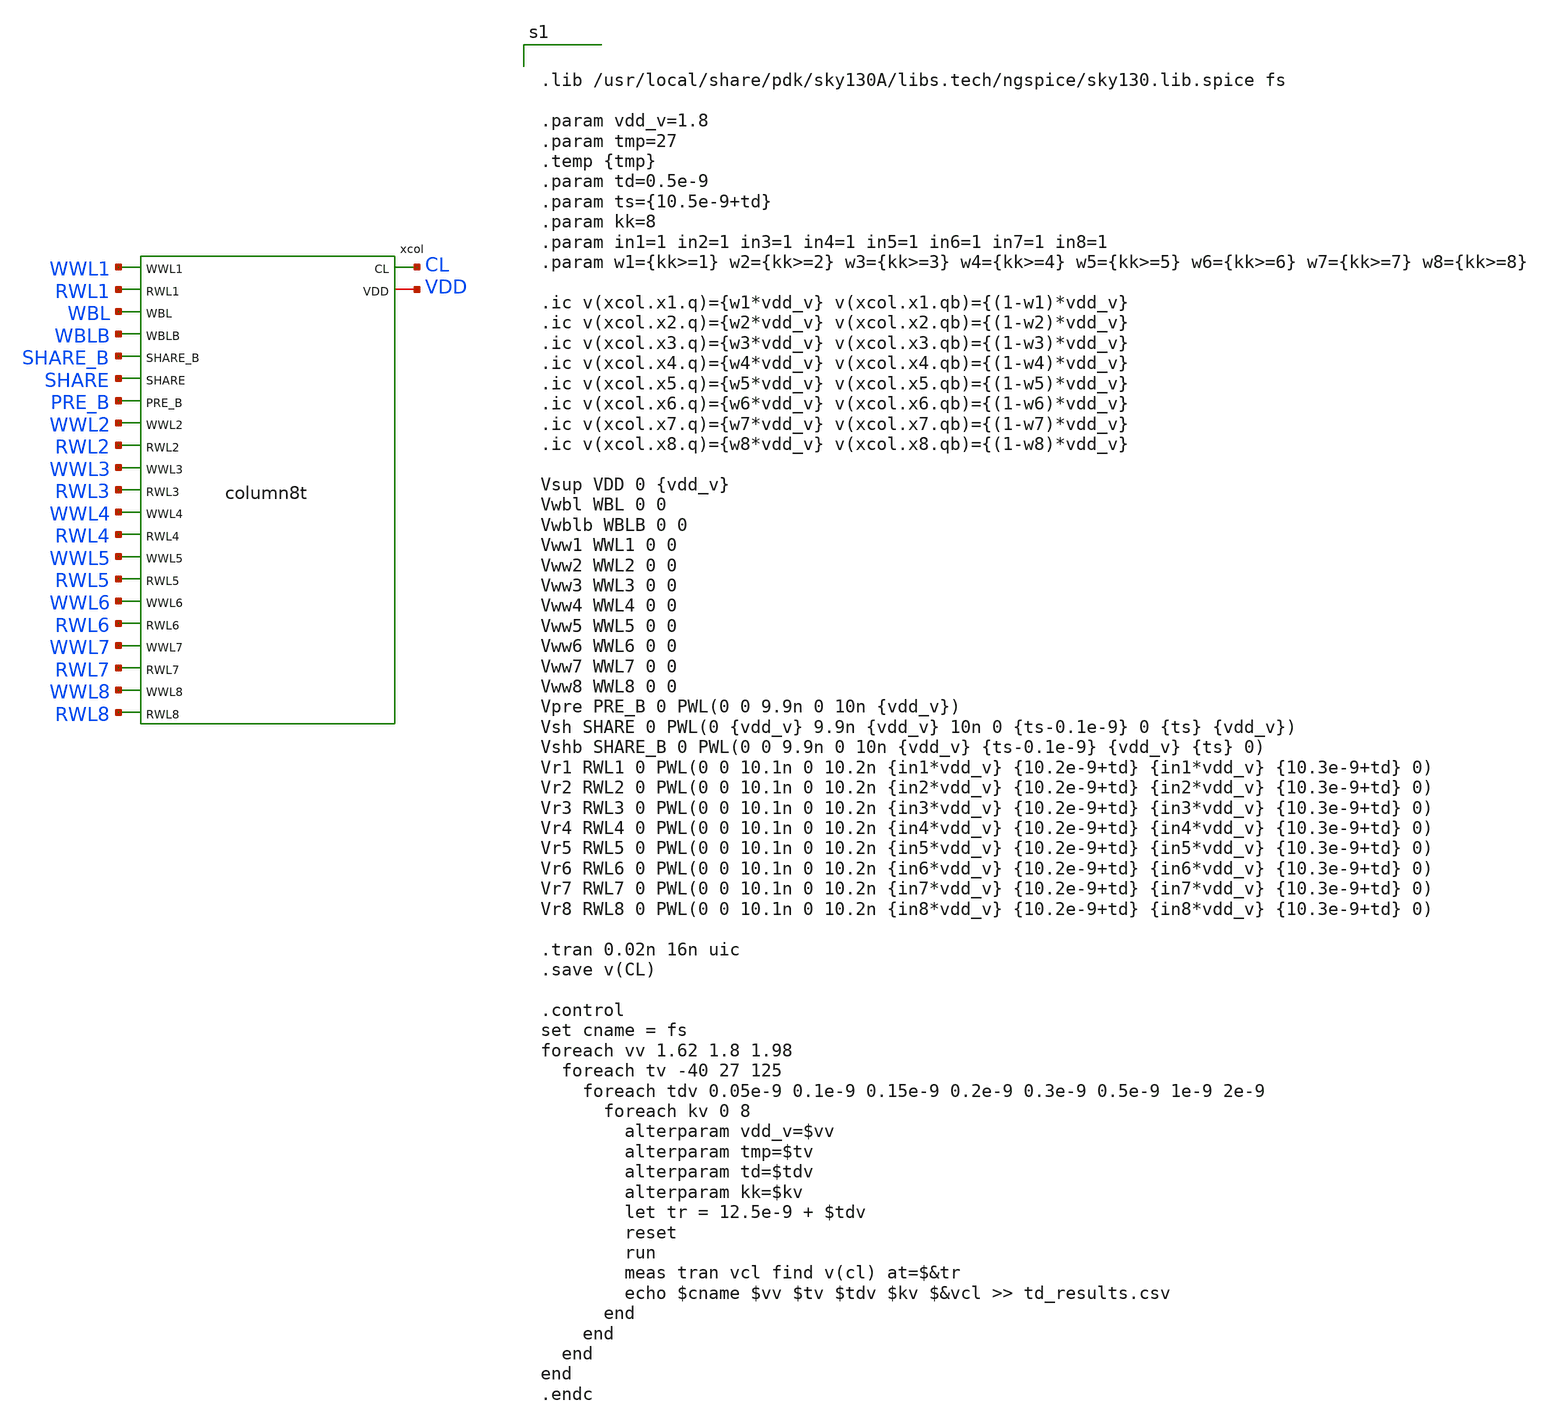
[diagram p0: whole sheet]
** sch_path: schematics/untitled-1.sch
**.subckt untitled-1
xcol CL VDD WWL1 RWL1 WBL WBLB SHARE_B SHARE PRE_B WWL2 RWL2 WWL3 RWL3 WWL4 RWL4 WWL5 RWL5 WWL6 RWL6
+ WWL7 RWL7 WWL8 RWL8 column8t
**** begin user architecture code


.lib /usr/local/share/pdk/sky130A/libs.tech/ngspice/sky130.lib.spice fs

.param vdd_v=1.8
.param tmp=27
.temp {tmp}
.param td=0.5e-9
.param ts={10.5e-9+td}
.param kk=8
.param in1=1 in2=1 in3=1 in4=1 in5=1 in6=1 in7=1 in8=1
.param w1={kk>=1} w2={kk>=2} w3={kk>=3} w4={kk>=4} w5={kk>=5} w6={kk>=6} w7={kk>=7} w8={kk>=8}

.ic v(xcol.x1.q)={w1*vdd_v} v(xcol.x1.qb)={(1-w1)*vdd_v}
.ic v(xcol.x2.q)={w2*vdd_v} v(xcol.x2.qb)={(1-w2)*vdd_v}
.ic v(xcol.x3.q)={w3*vdd_v} v(xcol.x3.qb)={(1-w3)*vdd_v}
.ic v(xcol.x4.q)={w4*vdd_v} v(xcol.x4.qb)={(1-w4)*vdd_v}
.ic v(xcol.x5.q)={w5*vdd_v} v(xcol.x5.qb)={(1-w5)*vdd_v}
.ic v(xcol.x6.q)={w6*vdd_v} v(xcol.x6.qb)={(1-w6)*vdd_v}
.ic v(xcol.x7.q)={w7*vdd_v} v(xcol.x7.qb)={(1-w7)*vdd_v}
.ic v(xcol.x8.q)={w8*vdd_v} v(xcol.x8.qb)={(1-w8)*vdd_v}

Vsup VDD 0 {vdd_v}
Vwbl WBL 0 0
Vwblb WBLB 0 0
Vww1 WWL1 0 0
Vww2 WWL2 0 0
Vww3 WWL3 0 0
Vww4 WWL4 0 0
Vww5 WWL5 0 0
Vww6 WWL6 0 0
Vww7 WWL7 0 0
Vww8 WWL8 0 0
Vpre PRE_B 0 PWL(0 0 9.9n 0 10n {vdd_v})
Vsh SHARE 0 PWL(0 {vdd_v} 9.9n {vdd_v} 10n 0 {ts-0.1e-9} 0 {ts} {vdd_v})
Vshb SHARE_B 0 PWL(0 0 9.9n 0 10n {vdd_v} {ts-0.1e-9} {vdd_v} {ts} 0)
Vr1 RWL1 0 PWL(0 0 10.1n 0 10.2n {in1*vdd_v} {10.2e-9+td} {in1*vdd_v} {10.3e-9+td} 0)
Vr2 RWL2 0 PWL(0 0 10.1n 0 10.2n {in2*vdd_v} {10.2e-9+td} {in2*vdd_v} {10.3e-9+td} 0)
Vr3 RWL3 0 PWL(0 0 10.1n 0 10.2n {in3*vdd_v} {10.2e-9+td} {in3*vdd_v} {10.3e-9+td} 0)
Vr4 RWL4 0 PWL(0 0 10.1n 0 10.2n {in4*vdd_v} {10.2e-9+td} {in4*vdd_v} {10.3e-9+td} 0)
Vr5 RWL5 0 PWL(0 0 10.1n 0 10.2n {in5*vdd_v} {10.2e-9+td} {in5*vdd_v} {10.3e-9+td} 0)
Vr6 RWL6 0 PWL(0 0 10.1n 0 10.2n {in6*vdd_v} {10.2e-9+td} {in6*vdd_v} {10.3e-9+td} 0)
Vr7 RWL7 0 PWL(0 0 10.1n 0 10.2n {in7*vdd_v} {10.2e-9+td} {in7*vdd_v} {10.3e-9+td} 0)
Vr8 RWL8 0 PWL(0 0 10.1n 0 10.2n {in8*vdd_v} {10.2e-9+td} {in8*vdd_v} {10.3e-9+td} 0)

.tran 0.02n 16n uic
.save v(CL)

.control
set cname = fs
foreach vv 1.62 1.8 1.98
  foreach tv -40 27 125
    foreach tdv 0.05e-9 0.1e-9 0.15e-9 0.2e-9 0.3e-9 0.5e-9 1e-9 2e-9
      foreach kv 0 8
        alterparam vdd_v=$vv
        alterparam tmp=$tv
        alterparam td=$tdv
        alterparam kk=$kv
        let tr = 12.5e-9 + $tdv
        reset
        run
        meas tran vcl find v(cl) at=$&tr
        echo $cname $vv $tv $tdv $kv $&vcl >> td_results.csv
      end
    end
  end
end
.endc


**** end user architecture code
**.ends
.end
